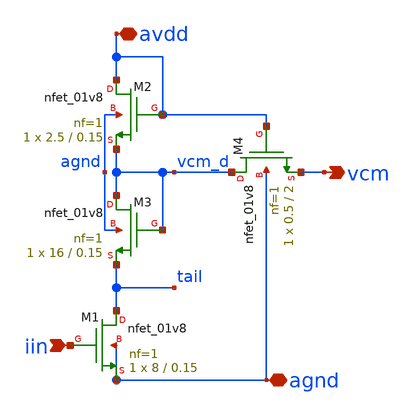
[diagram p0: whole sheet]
** sch_path: AMP/Hard_CM_Injector_0v8.sch
**.subckt Hard_CM_Injector_0v8 avdd vcm agnd iin
*.iopin avdd
*.opin vcm
*.iopin agnd
*.ipin iin
XM1 tail iin agnd agnd sky130_fd_pr__nfet_01v8 L=0.15 W=8 nf=1 ad='int((nf+1)/2) * W/nf * 0.29' as='int((nf+2)/2) * W/nf * 0.29'
+ pd='2*int((nf+1)/2) * (W/nf + 0.29)' ps='2*int((nf+2)/2) * (W/nf + 0.29)' nrd='0.29 / W' nrs='0.29 / W'
+ sa=0 sb=0 sd=0 mult=1 m=1
XM2 avdd avdd vcm_d agnd sky130_fd_pr__nfet_01v8 L=0.15 W=2.5 nf=1 ad='int((nf+1)/2) * W/nf * 0.29' as='int((nf+2)/2) * W/nf * 0.29'
+ pd='2*int((nf+1)/2) * (W/nf + 0.29)' ps='2*int((nf+2)/2) * (W/nf + 0.29)' nrd='0.29 / W' nrs='0.29 / W'
+ sa=0 sb=0 sd=0 mult=1 m=1
XM3 vcm_d vcm_d tail agnd sky130_fd_pr__nfet_01v8 L=0.15 W=16 nf=1 ad='int((nf+1)/2) * W/nf * 0.29' as='int((nf+2)/2) * W/nf * 0.29'
+ pd='2*int((nf+1)/2) * (W/nf + 0.29)' ps='2*int((nf+2)/2) * (W/nf + 0.29)' nrd='0.29 / W' nrs='0.29 / W'
+ sa=0 sb=0 sd=0 mult=1 m=1
XM4 vcm_d avdd vcm agnd sky130_fd_pr__nfet_01v8 L=2 W=0.5 nf=1 ad='int((nf+1)/2) * W/nf * 0.29' as='int((nf+2)/2) * W/nf * 0.29'
+ pd='2*int((nf+1)/2) * (W/nf + 0.29)' ps='2*int((nf+2)/2) * (W/nf + 0.29)' nrd='0.29 / W' nrs='0.29 / W'
+ sa=0 sb=0 sd=0 mult=1 m=1
**.ends
.end
